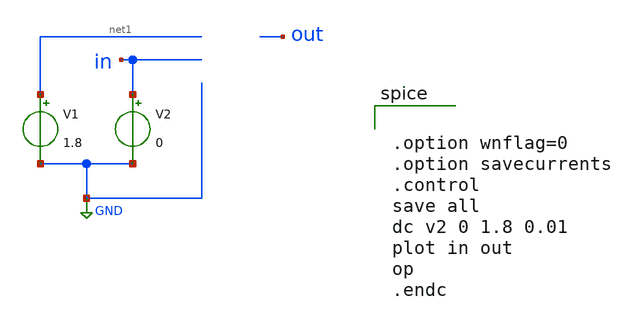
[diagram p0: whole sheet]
** sch_path: Inverter/inverter1.sch
**.subckt inverter1
V1 net1 GND 1.8
V2 in GND 0
**** begin user architecture code


.option wnflag=0
.option savecurrents
.control
save all
dc v2 0 1.8 0.01
plot in out
op
.endc



** opencircuitdesign pdks install
.lib $::SKYWATER_MODELS/sky130.lib.spice tt

**** end user architecture code
**.ends
.GLOBAL GND
.end
